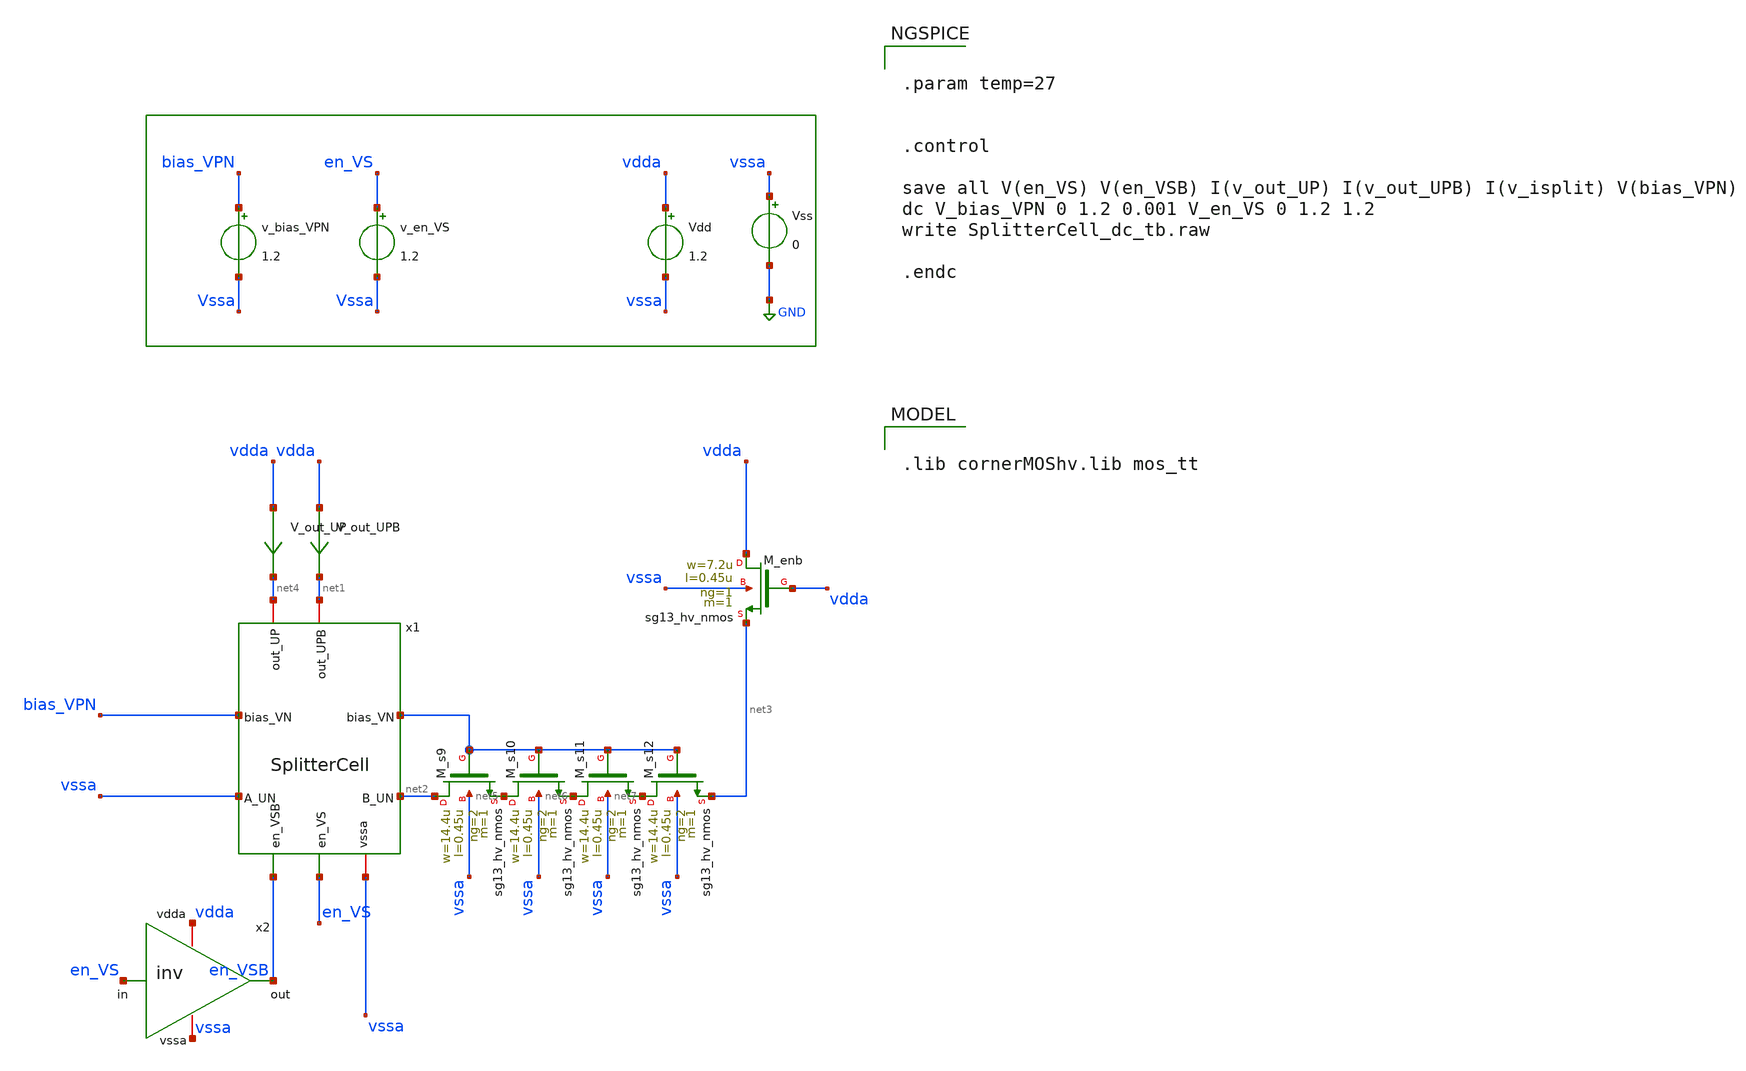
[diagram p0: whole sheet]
** sch_path: test_bench/SplitterCell_dc_tb.sch
**.subckt SplitterCell_dc_tb
x1 en_VS vssa net2 en_VSB bias_VPN vssa net1 net4 SplitterCell
v_bias_VPN bias_VPN Vssa 1.2
Vdd vdda vssa 1.2
v_en_VS en_VS Vssa 1.2
Vss vssa GND 0
XM_enb vdda vdda net3 vssa sg13_hv_nmos w=7.2u l=0.45u ng=1 m=1 mm_ok=1
XM_s9 net2 bias_VPN net5 vssa sg13_hv_nmos w=14.4u l=0.45u ng=2 m=1 mm_ok=1
XM_s10 net5 bias_VPN net6 vssa sg13_hv_nmos w=14.4u l=0.45u ng=2 m=1 mm_ok=1
XM_s11 net6 bias_VPN net7 vssa sg13_hv_nmos w=14.4u l=0.45u ng=2 m=1 mm_ok=1
XM_s12 net7 bias_VPN net3 vssa sg13_hv_nmos w=14.4u l=0.45u ng=2 m=1 mm_ok=1
x2 vdda en_VSB en_VS vssa inv
V_out_UPB vdda net1 0
.save i(v_out_upb)
V_out_UP vdda net4 0
.save i(v_out_up)
**** begin user architecture code

.lib cornerMOShv.lib mos_tt



.param temp=27


.control

save all V(en_VS) V(en_VSB) I(v_out_UP) I(v_out_UPB) I(v_isplit) V(bias_VPN)
dc V_bias_VPN 0 1.2 0.001 V_en_VS 0 1.2 1.2
write SplitterCell_dc_tb.raw

.endc


**** end user architecture code
**.ends
.GLOBAL GND
.end
